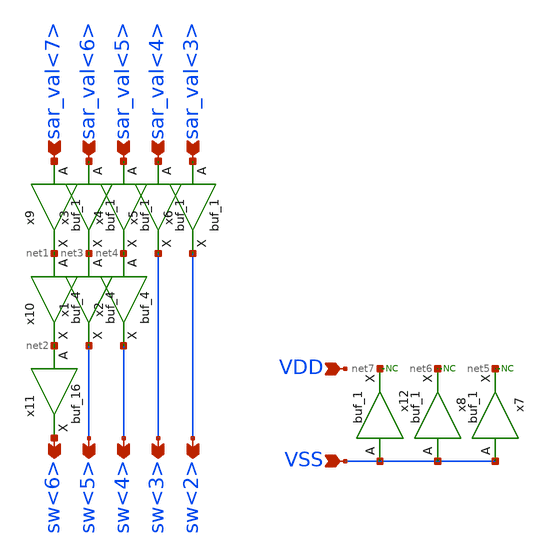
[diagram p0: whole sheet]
** sch_path: hgu/xschem/hgu_cdac_sw_buffer.sch
**.subckt hgu_cdac_sw_buffer sar_val<7> sw<6> sw<5> sw<4> sw<3> sw<2> sar_val<6> sar_val<5>
*+ sar_val<4> sar_val<3> VDD VSS
*.ipin sar_val<7>
*.opin sw<6>
*.opin sw<5>
*.opin sw<4>
*.opin sw<3>
*.opin sw<2>
*.ipin sar_val<6>
*.ipin sar_val<5>
*.ipin sar_val<4>
*.ipin sar_val<3>
*.ipin VDD
*.ipin VSS
x9 sar_val<7> VSS VSS VDD VDD net1 sky130_fd_sc_hd__buf_1
x10 net1 VSS VSS VDD VDD net2 sky130_fd_sc_hd__buf_4
x11 net2 VSS VSS VDD VDD sw<6> sky130_fd_sc_hd__buf_16
x1 net3 VSS VSS VDD VDD sw<5> sky130_fd_sc_hd__buf_4
x2 net4 VSS VSS VDD VDD sw<4> sky130_fd_sc_hd__buf_4
x3 sar_val<6> VSS VSS VDD VDD net3 sky130_fd_sc_hd__buf_1
x4 sar_val<5> VSS VSS VDD VDD net4 sky130_fd_sc_hd__buf_1
x5 sar_val<4> VSS VSS VDD VDD sw<3> sky130_fd_sc_hd__buf_1
x6 sar_val<3> VSS VSS VDD VDD sw<2> sky130_fd_sc_hd__buf_1
x7 VSS VSS VSS VDD VDD net5 sky130_fd_sc_hd__buf_1
x8 VSS VSS VSS VDD VDD net6 sky130_fd_sc_hd__buf_1
x12 VSS VSS VSS VDD VDD net7 sky130_fd_sc_hd__buf_1
* noconn #net7
* noconn #net6
* noconn #net5
**.ends
.end
